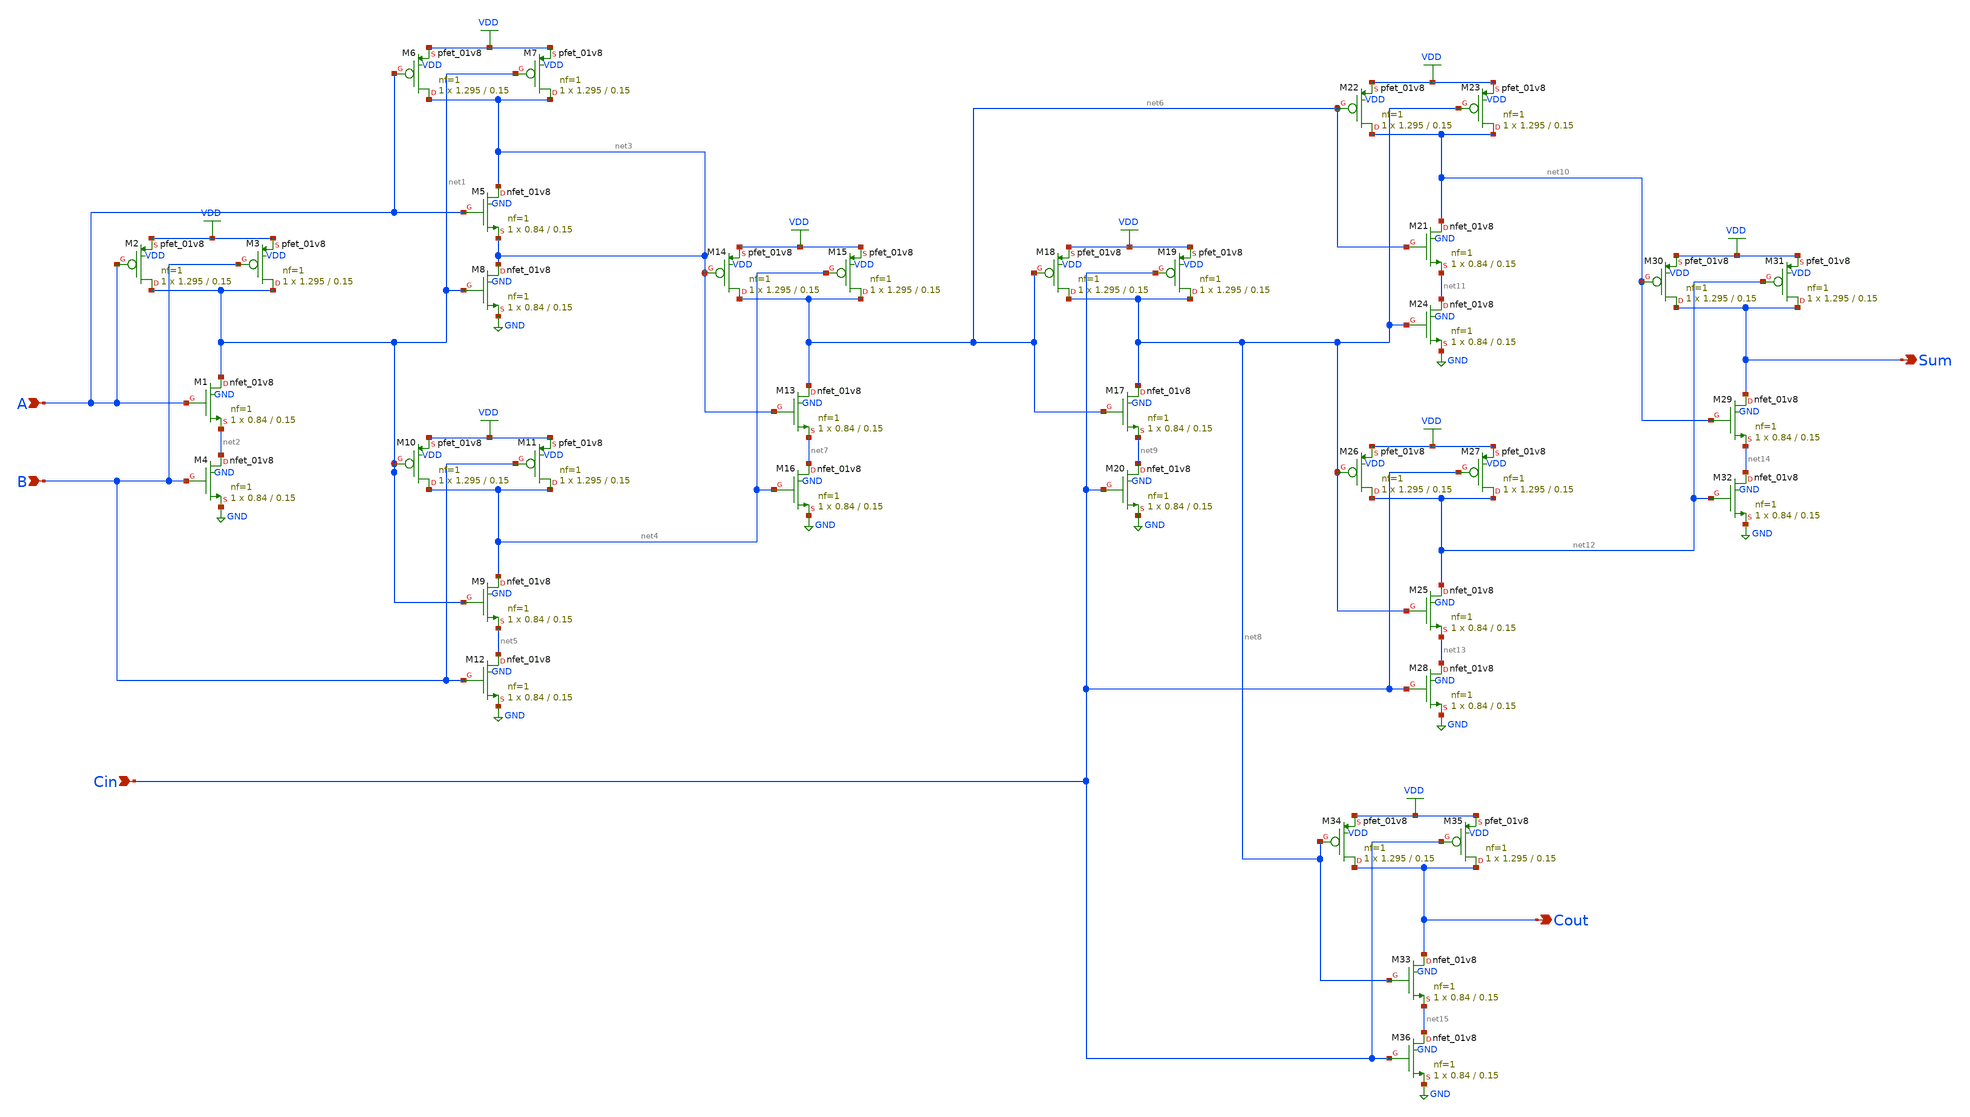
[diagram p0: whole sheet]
** sch_path: logicaleffort/fulladder.sch
**.subckt fulladder A B Cin Cout Sum
*.ipin A
*.ipin B
*.ipin Cin
*.opin Cout
*.opin Sum
XM1 net1 A net2 GND sky130_fd_pr__nfet_01v8 L=0.15 W=0.84 nf=1 ad='int((1 + 1)/2) * 0.84 / 1 * 0.29'
+ as='int((1 + 2)/2) * 0.84 / 1 * 0.29' pd='2*int((1 + 1)/2) * (0.84 / 1 + 0.29)' ps='2*int((1 + 2)/2) * (0.84 / 1 + 0.29)'
+ nrd='0.29 / 0.84 ' nrs='0.29 / 0.84 ' sa=0 sb=0 sd=0 mult=1 m=1
XM2 net1 A VDD VDD sky130_fd_pr__pfet_01v8 L=0.15 W=1.295 nf=1 ad='int((1 + 1)/2) * 1.295 / 1 * 0.29'
+ as='int((1 + 2)/2) * 1.295 / 1 * 0.29' pd='2*int((1 + 1)/2) * (1.295 / 1 + 0.29)' ps='2*int((1 + 2)/2) * (1.295 / 1 + 0.29)'
+ nrd='0.29 / 1.295 ' nrs='0.29 / 1.295 ' sa=0 sb=0 sd=0 mult=1 m=1
XM3 net1 B VDD VDD sky130_fd_pr__pfet_01v8 L=0.15 W=1.295 nf=1 ad='int((1 + 1)/2) * 1.295 / 1 * 0.29'
+ as='int((1 + 2)/2) * 1.295 / 1 * 0.29' pd='2*int((1 + 1)/2) * (1.295 / 1 + 0.29)' ps='2*int((1 + 2)/2) * (1.295 / 1 + 0.29)'
+ nrd='0.29 / 1.295 ' nrs='0.29 / 1.295 ' sa=0 sb=0 sd=0 mult=1 m=1
XM4 net2 B GND GND sky130_fd_pr__nfet_01v8 L=0.15 W=0.84 nf=1 ad='int((1 + 1)/2) * 0.84 / 1 * 0.29' as='int((1 + 2)/2) * 0.84 / 1 * 0.29'
+ pd='2*int((1 + 1)/2) * (0.84 / 1 + 0.29)' ps='2*int((1 + 2)/2) * (0.84 / 1 + 0.29)' nrd='0.29 / 0.84 '
+ nrs='0.29 / 0.84 ' sa=0 sb=0 sd=0 mult=1 m=1
XM5 net3 A net3 GND sky130_fd_pr__nfet_01v8 L=0.15 W=0.84 nf=1 ad='int((1 + 1)/2) * 0.84 / 1 * 0.29'
+ as='int((1 + 2)/2) * 0.84 / 1 * 0.29' pd='2*int((1 + 1)/2) * (0.84 / 1 + 0.29)' ps='2*int((1 + 2)/2) * (0.84 / 1 + 0.29)'
+ nrd='0.29 / 0.84 ' nrs='0.29 / 0.84 ' sa=0 sb=0 sd=0 mult=1 m=1
XM6 net3 A VDD VDD sky130_fd_pr__pfet_01v8 L=0.15 W=1.295 nf=1 ad='int((1 + 1)/2) * 1.295 / 1 * 0.29'
+ as='int((1 + 2)/2) * 1.295 / 1 * 0.29' pd='2*int((1 + 1)/2) * (1.295 / 1 + 0.29)' ps='2*int((1 + 2)/2) * (1.295 / 1 + 0.29)'
+ nrd='0.29 / 1.295 ' nrs='0.29 / 1.295 ' sa=0 sb=0 sd=0 mult=1 m=1
XM7 net3 net1 VDD VDD sky130_fd_pr__pfet_01v8 L=0.15 W=1.295 nf=1 ad='int((1 + 1)/2) * 1.295 / 1 * 0.29'
+ as='int((1 + 2)/2) * 1.295 / 1 * 0.29' pd='2*int((1 + 1)/2) * (1.295 / 1 + 0.29)' ps='2*int((1 + 2)/2) * (1.295 / 1 + 0.29)'
+ nrd='0.29 / 1.295 ' nrs='0.29 / 1.295 ' sa=0 sb=0 sd=0 mult=1 m=1
XM8 net3 net1 GND GND sky130_fd_pr__nfet_01v8 L=0.15 W=0.84 nf=1 ad='int((1 + 1)/2) * 0.84 / 1 * 0.29'
+ as='int((1 + 2)/2) * 0.84 / 1 * 0.29' pd='2*int((1 + 1)/2) * (0.84 / 1 + 0.29)' ps='2*int((1 + 2)/2) * (0.84 / 1 + 0.29)'
+ nrd='0.29 / 0.84 ' nrs='0.29 / 0.84 ' sa=0 sb=0 sd=0 mult=1 m=1
XM9 net4 net1 net5 GND sky130_fd_pr__nfet_01v8 L=0.15 W=0.84 nf=1 ad='int((1 + 1)/2) * 0.84 / 1 * 0.29'
+ as='int((1 + 2)/2) * 0.84 / 1 * 0.29' pd='2*int((1 + 1)/2) * (0.84 / 1 + 0.29)' ps='2*int((1 + 2)/2) * (0.84 / 1 + 0.29)'
+ nrd='0.29 / 0.84 ' nrs='0.29 / 0.84 ' sa=0 sb=0 sd=0 mult=1 m=1
XM10 net4 net1 VDD VDD sky130_fd_pr__pfet_01v8 L=0.15 W=1.295 nf=1 ad='int((1 + 1)/2) * 1.295 / 1 * 0.29'
+ as='int((1 + 2)/2) * 1.295 / 1 * 0.29' pd='2*int((1 + 1)/2) * (1.295 / 1 + 0.29)' ps='2*int((1 + 2)/2) * (1.295 / 1 + 0.29)'
+ nrd='0.29 / 1.295 ' nrs='0.29 / 1.295 ' sa=0 sb=0 sd=0 mult=1 m=1
XM11 net4 B VDD VDD sky130_fd_pr__pfet_01v8 L=0.15 W=1.295 nf=1 ad='int((1 + 1)/2) * 1.295 / 1 * 0.29'
+ as='int((1 + 2)/2) * 1.295 / 1 * 0.29' pd='2*int((1 + 1)/2) * (1.295 / 1 + 0.29)' ps='2*int((1 + 2)/2) * (1.295 / 1 + 0.29)'
+ nrd='0.29 / 1.295 ' nrs='0.29 / 1.295 ' sa=0 sb=0 sd=0 mult=1 m=1
XM12 net5 B GND GND sky130_fd_pr__nfet_01v8 L=0.15 W=0.84 nf=1 ad='int((1 + 1)/2) * 0.84 / 1 * 0.29'
+ as='int((1 + 2)/2) * 0.84 / 1 * 0.29' pd='2*int((1 + 1)/2) * (0.84 / 1 + 0.29)' ps='2*int((1 + 2)/2) * (0.84 / 1 + 0.29)'
+ nrd='0.29 / 0.84 ' nrs='0.29 / 0.84 ' sa=0 sb=0 sd=0 mult=1 m=1
XM13 net6 net3 net7 GND sky130_fd_pr__nfet_01v8 L=0.15 W=0.84 nf=1 ad='int((1 + 1)/2) * 0.84 / 1 * 0.29'
+ as='int((1 + 2)/2) * 0.84 / 1 * 0.29' pd='2*int((1 + 1)/2) * (0.84 / 1 + 0.29)' ps='2*int((1 + 2)/2) * (0.84 / 1 + 0.29)'
+ nrd='0.29 / 0.84 ' nrs='0.29 / 0.84 ' sa=0 sb=0 sd=0 mult=1 m=1
XM14 net6 net3 VDD VDD sky130_fd_pr__pfet_01v8 L=0.15 W=1.295 nf=1 ad='int((1 + 1)/2) * 1.295 / 1 * 0.29'
+ as='int((1 + 2)/2) * 1.295 / 1 * 0.29' pd='2*int((1 + 1)/2) * (1.295 / 1 + 0.29)' ps='2*int((1 + 2)/2) * (1.295 / 1 + 0.29)'
+ nrd='0.29 / 1.295 ' nrs='0.29 / 1.295 ' sa=0 sb=0 sd=0 mult=1 m=1
XM15 net6 net4 VDD VDD sky130_fd_pr__pfet_01v8 L=0.15 W=1.295 nf=1 ad='int((1 + 1)/2) * 1.295 / 1 * 0.29'
+ as='int((1 + 2)/2) * 1.295 / 1 * 0.29' pd='2*int((1 + 1)/2) * (1.295 / 1 + 0.29)' ps='2*int((1 + 2)/2) * (1.295 / 1 + 0.29)'
+ nrd='0.29 / 1.295 ' nrs='0.29 / 1.295 ' sa=0 sb=0 sd=0 mult=1 m=1
XM16 net7 net4 GND GND sky130_fd_pr__nfet_01v8 L=0.15 W=0.84 nf=1 ad='int((1 + 1)/2) * 0.84 / 1 * 0.29'
+ as='int((1 + 2)/2) * 0.84 / 1 * 0.29' pd='2*int((1 + 1)/2) * (0.84 / 1 + 0.29)' ps='2*int((1 + 2)/2) * (0.84 / 1 + 0.29)'
+ nrd='0.29 / 0.84 ' nrs='0.29 / 0.84 ' sa=0 sb=0 sd=0 mult=1 m=1
XM17 net8 net6 net9 GND sky130_fd_pr__nfet_01v8 L=0.15 W=0.84 nf=1 ad='int((1 + 1)/2) * 0.84 / 1 * 0.29'
+ as='int((1 + 2)/2) * 0.84 / 1 * 0.29' pd='2*int((1 + 1)/2) * (0.84 / 1 + 0.29)' ps='2*int((1 + 2)/2) * (0.84 / 1 + 0.29)'
+ nrd='0.29 / 0.84 ' nrs='0.29 / 0.84 ' sa=0 sb=0 sd=0 mult=1 m=1
XM18 net8 net6 VDD VDD sky130_fd_pr__pfet_01v8 L=0.15 W=1.295 nf=1 ad='int((1 + 1)/2) * 1.295 / 1 * 0.29'
+ as='int((1 + 2)/2) * 1.295 / 1 * 0.29' pd='2*int((1 + 1)/2) * (1.295 / 1 + 0.29)' ps='2*int((1 + 2)/2) * (1.295 / 1 + 0.29)'
+ nrd='0.29 / 1.295 ' nrs='0.29 / 1.295 ' sa=0 sb=0 sd=0 mult=1 m=1
XM19 net8 Cin VDD VDD sky130_fd_pr__pfet_01v8 L=0.15 W=1.295 nf=1 ad='int((1 + 1)/2) * 1.295 / 1 * 0.29'
+ as='int((1 + 2)/2) * 1.295 / 1 * 0.29' pd='2*int((1 + 1)/2) * (1.295 / 1 + 0.29)' ps='2*int((1 + 2)/2) * (1.295 / 1 + 0.29)'
+ nrd='0.29 / 1.295 ' nrs='0.29 / 1.295 ' sa=0 sb=0 sd=0 mult=1 m=1
XM20 net9 Cin GND GND sky130_fd_pr__nfet_01v8 L=0.15 W=0.84 nf=1 ad='int((1 + 1)/2) * 0.84 / 1 * 0.29'
+ as='int((1 + 2)/2) * 0.84 / 1 * 0.29' pd='2*int((1 + 1)/2) * (0.84 / 1 + 0.29)' ps='2*int((1 + 2)/2) * (0.84 / 1 + 0.29)'
+ nrd='0.29 / 0.84 ' nrs='0.29 / 0.84 ' sa=0 sb=0 sd=0 mult=1 m=1
XM21 net10 net6 net11 GND sky130_fd_pr__nfet_01v8 L=0.15 W=0.84 nf=1 ad='int((1 + 1)/2) * 0.84 / 1 * 0.29'
+ as='int((1 + 2)/2) * 0.84 / 1 * 0.29' pd='2*int((1 + 1)/2) * (0.84 / 1 + 0.29)' ps='2*int((1 + 2)/2) * (0.84 / 1 + 0.29)'
+ nrd='0.29 / 0.84 ' nrs='0.29 / 0.84 ' sa=0 sb=0 sd=0 mult=1 m=1
XM22 net10 net6 VDD VDD sky130_fd_pr__pfet_01v8 L=0.15 W=1.295 nf=1 ad='int((1 + 1)/2) * 1.295 / 1 * 0.29'
+ as='int((1 + 2)/2) * 1.295 / 1 * 0.29' pd='2*int((1 + 1)/2) * (1.295 / 1 + 0.29)' ps='2*int((1 + 2)/2) * (1.295 / 1 + 0.29)'
+ nrd='0.29 / 1.295 ' nrs='0.29 / 1.295 ' sa=0 sb=0 sd=0 mult=1 m=1
XM23 net10 net8 VDD VDD sky130_fd_pr__pfet_01v8 L=0.15 W=1.295 nf=1 ad='int((1 + 1)/2) * 1.295 / 1 * 0.29'
+ as='int((1 + 2)/2) * 1.295 / 1 * 0.29' pd='2*int((1 + 1)/2) * (1.295 / 1 + 0.29)' ps='2*int((1 + 2)/2) * (1.295 / 1 + 0.29)'
+ nrd='0.29 / 1.295 ' nrs='0.29 / 1.295 ' sa=0 sb=0 sd=0 mult=1 m=1
XM24 net11 net8 GND GND sky130_fd_pr__nfet_01v8 L=0.15 W=0.84 nf=1 ad='int((1 + 1)/2) * 0.84 / 1 * 0.29'
+ as='int((1 + 2)/2) * 0.84 / 1 * 0.29' pd='2*int((1 + 1)/2) * (0.84 / 1 + 0.29)' ps='2*int((1 + 2)/2) * (0.84 / 1 + 0.29)'
+ nrd='0.29 / 0.84 ' nrs='0.29 / 0.84 ' sa=0 sb=0 sd=0 mult=1 m=1
XM25 net12 net8 net13 GND sky130_fd_pr__nfet_01v8 L=0.15 W=0.84 nf=1 ad='int((1 + 1)/2) * 0.84 / 1 * 0.29'
+ as='int((1 + 2)/2) * 0.84 / 1 * 0.29' pd='2*int((1 + 1)/2) * (0.84 / 1 + 0.29)' ps='2*int((1 + 2)/2) * (0.84 / 1 + 0.29)'
+ nrd='0.29 / 0.84 ' nrs='0.29 / 0.84 ' sa=0 sb=0 sd=0 mult=1 m=1
XM26 net12 net8 VDD VDD sky130_fd_pr__pfet_01v8 L=0.15 W=1.295 nf=1 ad='int((1 + 1)/2) * 1.295 / 1 * 0.29'
+ as='int((1 + 2)/2) * 1.295 / 1 * 0.29' pd='2*int((1 + 1)/2) * (1.295 / 1 + 0.29)' ps='2*int((1 + 2)/2) * (1.295 / 1 + 0.29)'
+ nrd='0.29 / 1.295 ' nrs='0.29 / 1.295 ' sa=0 sb=0 sd=0 mult=1 m=1
XM27 net12 Cin VDD VDD sky130_fd_pr__pfet_01v8 L=0.15 W=1.295 nf=1 ad='int((1 + 1)/2) * 1.295 / 1 * 0.29'
+ as='int((1 + 2)/2) * 1.295 / 1 * 0.29' pd='2*int((1 + 1)/2) * (1.295 / 1 + 0.29)' ps='2*int((1 + 2)/2) * (1.295 / 1 + 0.29)'
+ nrd='0.29 / 1.295 ' nrs='0.29 / 1.295 ' sa=0 sb=0 sd=0 mult=1 m=1
XM28 net13 Cin GND GND sky130_fd_pr__nfet_01v8 L=0.15 W=0.84 nf=1 ad='int((1 + 1)/2) * 0.84 / 1 * 0.29'
+ as='int((1 + 2)/2) * 0.84 / 1 * 0.29' pd='2*int((1 + 1)/2) * (0.84 / 1 + 0.29)' ps='2*int((1 + 2)/2) * (0.84 / 1 + 0.29)'
+ nrd='0.29 / 0.84 ' nrs='0.29 / 0.84 ' sa=0 sb=0 sd=0 mult=1 m=1
XM29 Sum net10 net14 GND sky130_fd_pr__nfet_01v8 L=0.15 W=0.84 nf=1 ad='int((1 + 1)/2) * 0.84 / 1 * 0.29'
+ as='int((1 + 2)/2) * 0.84 / 1 * 0.29' pd='2*int((1 + 1)/2) * (0.84 / 1 + 0.29)' ps='2*int((1 + 2)/2) * (0.84 / 1 + 0.29)'
+ nrd='0.29 / 0.84 ' nrs='0.29 / 0.84 ' sa=0 sb=0 sd=0 mult=1 m=1
XM30 Sum net10 VDD VDD sky130_fd_pr__pfet_01v8 L=0.15 W=1.295 nf=1 ad='int((1 + 1)/2) * 1.295 / 1 * 0.29'
+ as='int((1 + 2)/2) * 1.295 / 1 * 0.29' pd='2*int((1 + 1)/2) * (1.295 / 1 + 0.29)' ps='2*int((1 + 2)/2) * (1.295 / 1 + 0.29)'
+ nrd='0.29 / 1.295 ' nrs='0.29 / 1.295 ' sa=0 sb=0 sd=0 mult=1 m=1
XM31 Sum net12 VDD VDD sky130_fd_pr__pfet_01v8 L=0.15 W=1.295 nf=1 ad='int((1 + 1)/2) * 1.295 / 1 * 0.29'
+ as='int((1 + 2)/2) * 1.295 / 1 * 0.29' pd='2*int((1 + 1)/2) * (1.295 / 1 + 0.29)' ps='2*int((1 + 2)/2) * (1.295 / 1 + 0.29)'
+ nrd='0.29 / 1.295 ' nrs='0.29 / 1.295 ' sa=0 sb=0 sd=0 mult=1 m=1
XM32 net14 net12 GND GND sky130_fd_pr__nfet_01v8 L=0.15 W=0.84 nf=1 ad='int((1 + 1)/2) * 0.84 / 1 * 0.29'
+ as='int((1 + 2)/2) * 0.84 / 1 * 0.29' pd='2*int((1 + 1)/2) * (0.84 / 1 + 0.29)' ps='2*int((1 + 2)/2) * (0.84 / 1 + 0.29)'
+ nrd='0.29 / 0.84 ' nrs='0.29 / 0.84 ' sa=0 sb=0 sd=0 mult=1 m=1
XM33 Cout net8 net15 GND sky130_fd_pr__nfet_01v8 L=0.15 W=0.84 nf=1 ad='int((1 + 1)/2) * 0.84 / 1 * 0.29'
+ as='int((1 + 2)/2) * 0.84 / 1 * 0.29' pd='2*int((1 + 1)/2) * (0.84 / 1 + 0.29)' ps='2*int((1 + 2)/2) * (0.84 / 1 + 0.29)'
+ nrd='0.29 / 0.84 ' nrs='0.29 / 0.84 ' sa=0 sb=0 sd=0 mult=1 m=1
XM34 Cout net8 VDD VDD sky130_fd_pr__pfet_01v8 L=0.15 W=1.295 nf=1 ad='int((1 + 1)/2) * 1.295 / 1 * 0.29'
+ as='int((1 + 2)/2) * 1.295 / 1 * 0.29' pd='2*int((1 + 1)/2) * (1.295 / 1 + 0.29)' ps='2*int((1 + 2)/2) * (1.295 / 1 + 0.29)'
+ nrd='0.29 / 1.295 ' nrs='0.29 / 1.295 ' sa=0 sb=0 sd=0 mult=1 m=1
XM35 Cout Cin VDD VDD sky130_fd_pr__pfet_01v8 L=0.15 W=1.295 nf=1 ad='int((1 + 1)/2) * 1.295 / 1 * 0.29'
+ as='int((1 + 2)/2) * 1.295 / 1 * 0.29' pd='2*int((1 + 1)/2) * (1.295 / 1 + 0.29)' ps='2*int((1 + 2)/2) * (1.295 / 1 + 0.29)'
+ nrd='0.29 / 1.295 ' nrs='0.29 / 1.295 ' sa=0 sb=0 sd=0 mult=1 m=1
XM36 net15 Cin GND GND sky130_fd_pr__nfet_01v8 L=0.15 W=0.84 nf=1 ad='int((1 + 1)/2) * 0.84 / 1 * 0.29'
+ as='int((1 + 2)/2) * 0.84 / 1 * 0.29' pd='2*int((1 + 1)/2) * (0.84 / 1 + 0.29)' ps='2*int((1 + 2)/2) * (0.84 / 1 + 0.29)'
+ nrd='0.29 / 0.84 ' nrs='0.29 / 0.84 ' sa=0 sb=0 sd=0 mult=1 m=1
**.ends
.GLOBAL GND
.GLOBAL VDD
.end
